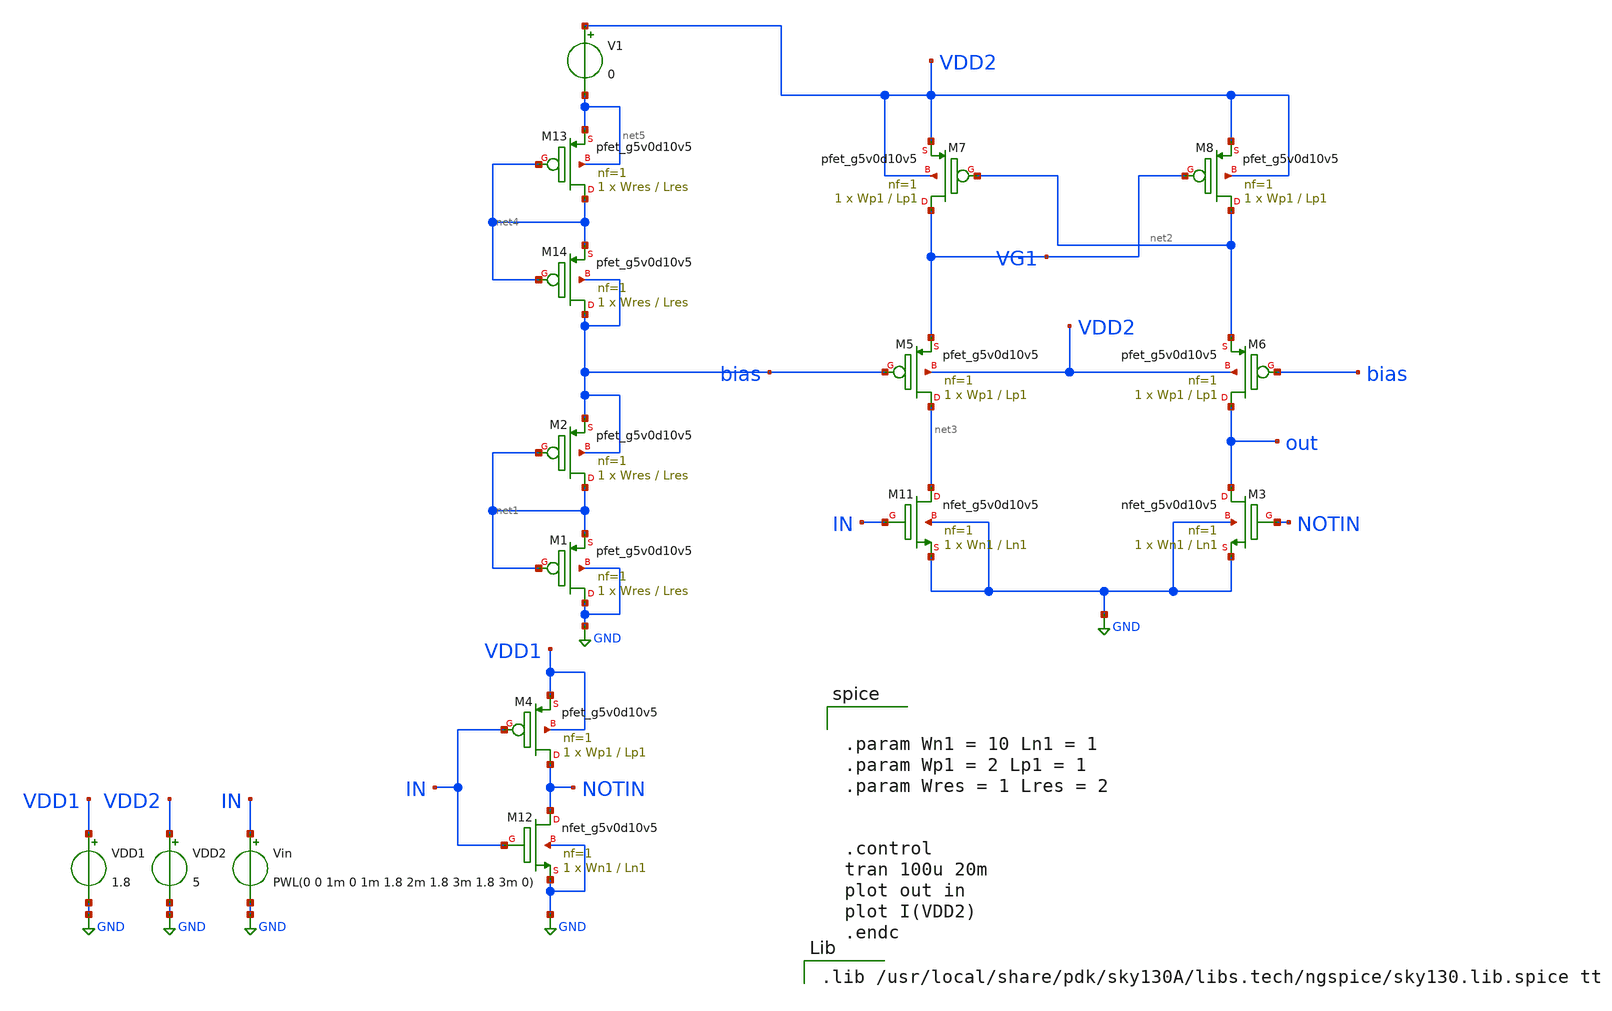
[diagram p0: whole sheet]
** sch_path: xschem/LevelShifiter.sch
**.subckt LevelShifiter
XM2 net1 net1 bias bias sky130_fd_pr__pfet_g5v0d10v5 L=Lres W=Wres nf=1 ad='int((nf+1)/2) * W/nf * 0.29'
+ as='int((nf+2)/2) * W/nf * 0.29' pd='2*int((nf+1)/2) * (W/nf + 0.29)' ps='2*int((nf+2)/2) * (W/nf + 0.29)'
+ nrd='0.29 / W' nrs='0.29 / W' sa=0 sb=0 sd=0 mult=1 m=1
XM3 out NOTIN GND GND sky130_fd_pr__nfet_g5v0d10v5 L=Ln1 W=Wn1 nf=1 ad='int((nf+1)/2) * W/nf * 0.29'
+ as='int((nf+2)/2) * W/nf * 0.29' pd='2*int((nf+1)/2) * (W/nf + 0.29)' ps='2*int((nf+2)/2) * (W/nf + 0.29)'
+ nrd='0.29 / W' nrs='0.29 / W' sa=0 sb=0 sd=0 mult=1 m=1
XM4 NOTIN IN VDD1 VDD1 sky130_fd_pr__pfet_g5v0d10v5 L=Lp1 W=Wp1 nf=1 ad='int((nf+1)/2) * W/nf * 0.29'
+ as='int((nf+2)/2) * W/nf * 0.29' pd='2*int((nf+1)/2) * (W/nf + 0.29)' ps='2*int((nf+2)/2) * (W/nf + 0.29)'
+ nrd='0.29 / W' nrs='0.29 / W' sa=0 sb=0 sd=0 mult=1 m=1
XM7 VG1 net2 VDD2 VDD2 sky130_fd_pr__pfet_g5v0d10v5 L=Lp1 W=Wp1 nf=1 ad='int((nf+1)/2) * W/nf * 0.29'
+ as='int((nf+2)/2) * W/nf * 0.29' pd='2*int((nf+1)/2) * (W/nf + 0.29)' ps='2*int((nf+2)/2) * (W/nf + 0.29)'
+ nrd='0.29 / W' nrs='0.29 / W' sa=0 sb=0 sd=0 mult=1 m=1
XM8 net2 VG1 VDD2 VDD2 sky130_fd_pr__pfet_g5v0d10v5 L=Lp1 W=Wp1 nf=1 ad='int((nf+1)/2) * W/nf * 0.29'
+ as='int((nf+2)/2) * W/nf * 0.29' pd='2*int((nf+1)/2) * (W/nf + 0.29)' ps='2*int((nf+2)/2) * (W/nf + 0.29)'
+ nrd='0.29 / W' nrs='0.29 / W' sa=0 sb=0 sd=0 mult=1 m=1
VDD1 VDD1 GND 1.8
VDD2 VDD2 GND 5
Vin IN GND PWL(0 0 1m 0 1m 1.8 2m 1.8 3m 1.8 3m 0)
XM5 net3 bias VG1 VDD2 sky130_fd_pr__pfet_g5v0d10v5 L=Lp1 W=Wp1 nf=1 ad='int((nf+1)/2) * W/nf * 0.29'
+ as='int((nf+2)/2) * W/nf * 0.29' pd='2*int((nf+1)/2) * (W/nf + 0.29)' ps='2*int((nf+2)/2) * (W/nf + 0.29)'
+ nrd='0.29 / W' nrs='0.29 / W' sa=0 sb=0 sd=0 mult=1 m=1
XM6 out bias net2 VDD2 sky130_fd_pr__pfet_g5v0d10v5 L=Lp1 W=Wp1 nf=1 ad='int((nf+1)/2) * W/nf * 0.29'
+ as='int((nf+2)/2) * W/nf * 0.29' pd='2*int((nf+1)/2) * (W/nf + 0.29)' ps='2*int((nf+2)/2) * (W/nf + 0.29)'
+ nrd='0.29 / W' nrs='0.29 / W' sa=0 sb=0 sd=0 mult=1 m=1
XM11 net3 IN GND GND sky130_fd_pr__nfet_g5v0d10v5 L=Ln1 W=Wn1 nf=1 ad='int((nf+1)/2) * W/nf * 0.29' as='int((nf+2)/2) * W/nf * 0.29'
+ pd='2*int((nf+1)/2) * (W/nf + 0.29)' ps='2*int((nf+2)/2) * (W/nf + 0.29)' nrd='0.29 / W' nrs='0.29 / W'
+ sa=0 sb=0 sd=0 mult=1 m=1
XM12 NOTIN IN GND GND sky130_fd_pr__nfet_g5v0d10v5 L=Ln1 W=Wn1 nf=1 ad='int((nf+1)/2) * W/nf * 0.29'
+ as='int((nf+2)/2) * W/nf * 0.29' pd='2*int((nf+1)/2) * (W/nf + 0.29)' ps='2*int((nf+2)/2) * (W/nf + 0.29)'
+ nrd='0.29 / W' nrs='0.29 / W' sa=0 sb=0 sd=0 mult=1 m=1
XM1 GND net1 net1 GND sky130_fd_pr__pfet_g5v0d10v5 L=Lres W=Wres nf=1 ad='int((nf+1)/2) * W/nf * 0.29'
+ as='int((nf+2)/2) * W/nf * 0.29' pd='2*int((nf+1)/2) * (W/nf + 0.29)' ps='2*int((nf+2)/2) * (W/nf + 0.29)'
+ nrd='0.29 / W' nrs='0.29 / W' sa=0 sb=0 sd=0 mult=1 m=1
XM13 net4 net4 net5 net5 sky130_fd_pr__pfet_g5v0d10v5 L=Lres W=Wres nf=1 ad='int((nf+1)/2) * W/nf * 0.29'
+ as='int((nf+2)/2) * W/nf * 0.29' pd='2*int((nf+1)/2) * (W/nf + 0.29)' ps='2*int((nf+2)/2) * (W/nf + 0.29)'
+ nrd='0.29 / W' nrs='0.29 / W' sa=0 sb=0 sd=0 mult=1 m=1
XM14 bias net4 net4 bias sky130_fd_pr__pfet_g5v0d10v5 L=Lres W=Wres nf=1 ad='int((nf+1)/2) * W/nf * 0.29'
+ as='int((nf+2)/2) * W/nf * 0.29' pd='2*int((nf+1)/2) * (W/nf + 0.29)' ps='2*int((nf+2)/2) * (W/nf + 0.29)'
+ nrd='0.29 / W' nrs='0.29 / W' sa=0 sb=0 sd=0 mult=1 m=1
V1 VDD2 net5 0
**** begin user architecture code


.param Wn1 = 10 Ln1 = 1
.param Wp1 = 2 Lp1 = 1
.param Wres = 1 Lres = 2


.control
tran 100u 20m
plot out in
plot I(VDD2)
.endc


.lib /usr/local/share/pdk/sky130A/libs.tech/ngspice/sky130.lib.spice tt

**** end user architecture code
**.ends
.GLOBAL GND
.end
